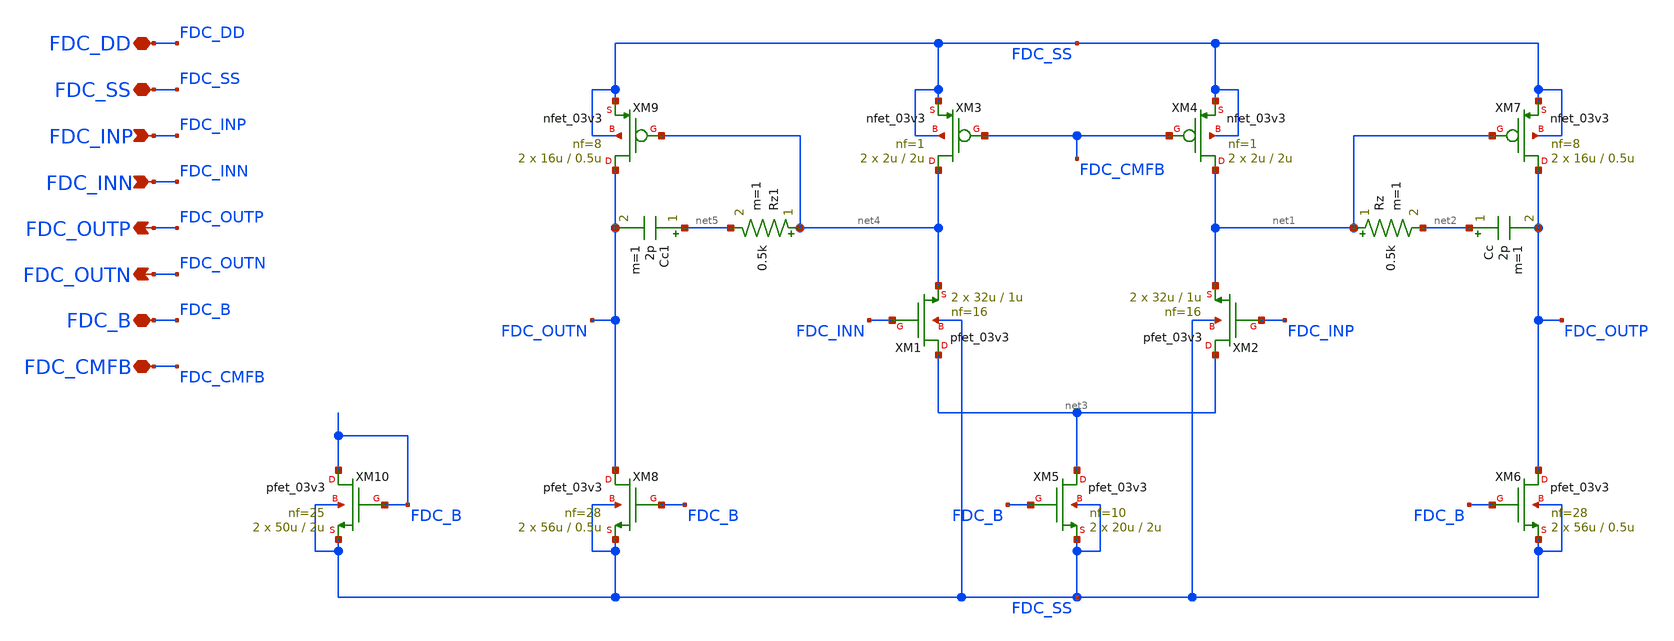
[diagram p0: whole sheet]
** sch_path: Design_Files/IC Design/Schematic/FD_OTA/FDC/FDC.sch
**.subckt FDC FDC_DD FDC_SS FDC_INP FDC_INN FDC_OUTP FDC_B FDC_OUTN FDC_CMFB
*.iopin FDC_DD
*.iopin FDC_SS
*.ipin FDC_INP
*.ipin FDC_INN
*.opin FDC_OUTP
*.iopin FDC_B
*.opin FDC_OUTN
*.iopin FDC_CMFB
XM4 net1 FDC_CMFB FDC_SS FDC_SS nfet_03v3 L=2u W=2u nf=1 ad='int((nf+1)/2) * W/nf * 0.18u' as='int((nf+2)/2) * W/nf * 0.18u'
+ pd='2*int((nf+1)/2) * (W/nf + 0.18u)' ps='2*int((nf+2)/2) * (W/nf + 0.18u)' nrd='0.18u / W' nrs='0.18u / W'
+ sa=0 sb=0 sd=0 m=2
XM3 net4 FDC_CMFB FDC_SS FDC_SS nfet_03v3 L=2u W=2u nf=1 ad='int((nf+1)/2) * W/nf * 0.18u' as='int((nf+2)/2) * W/nf * 0.18u'
+ pd='2*int((nf+1)/2) * (W/nf + 0.18u)' ps='2*int((nf+2)/2) * (W/nf + 0.18u)' nrd='0.18u / W' nrs='0.18u / W'
+ sa=0 sb=0 sd=0 m=2
XM1 net3 FDC_INN net4 FDC_SS pfet_03v3 L=1u W=32u nf=16 ad='int((nf+1)/2) * W/nf * 0.18u' as='int((nf+2)/2) * W/nf * 0.18u'
+ pd='2*int((nf+1)/2) * (W/nf + 0.18u)' ps='2*int((nf+2)/2) * (W/nf + 0.18u)' nrd='0.18u / W' nrs='0.18u / W'
+ sa=0 sb=0 sd=0 m=2
XM2 net3 FDC_INP net1 FDC_SS pfet_03v3 L=1u W=32u nf=16 ad='int((nf+1)/2) * W/nf * 0.18u' as='int((nf+2)/2) * W/nf * 0.18u'
+ pd='2*int((nf+1)/2) * (W/nf + 0.18u)' ps='2*int((nf+2)/2) * (W/nf + 0.18u)' nrd='0.18u / W' nrs='0.18u / W'
+ sa=0 sb=0 sd=0 m=2
XM6 FDC_OUTP FDC_B FDC_SS FDC_SS pfet_03v3 L=0.5u W=56u nf=28 ad='int((nf+1)/2) * W/nf * 0.18u' as='int((nf+2)/2) * W/nf * 0.18u'
+ pd='2*int((nf+1)/2) * (W/nf + 0.18u)' ps='2*int((nf+2)/2) * (W/nf + 0.18u)' nrd='0.18u / W' nrs='0.18u / W'
+ sa=0 sb=0 sd=0 m=2
Rz net1 net2 0.5k m=1
XM5 net3 FDC_B FDC_SS FDC_SS pfet_03v3 L=2u W=20u nf=10 ad='int((nf+1)/2) * W/nf * 0.18u' as='int((nf+2)/2) * W/nf * 0.18u'
+ pd='2*int((nf+1)/2) * (W/nf + 0.18u)' ps='2*int((nf+2)/2) * (W/nf + 0.18u)' nrd='0.18u / W' nrs='0.18u / W'
+ sa=0 sb=0 sd=0 m=2
XM7 FDC_OUTP net1 FDC_SS FDC_SS nfet_03v3 L=0.5u W=16u nf=8 ad='int((nf+1)/2) * W/nf * 0.18u' as='int((nf+2)/2) * W/nf * 0.18u'
+ pd='2*int((nf+1)/2) * (W/nf + 0.18u)' ps='2*int((nf+2)/2) * (W/nf + 0.18u)' nrd='0.18u / W' nrs='0.18u / W'
+ sa=0 sb=0 sd=0 m=2
XM10 FDC_B FDC_B FDC_SS FDC_SS pfet_03v3 L=2u W=50u nf=25 ad='int((nf+1)/2) * W/nf * 0.18u' as='int((nf+2)/2) * W/nf * 0.18u'
+ pd='2*int((nf+1)/2) * (W/nf + 0.18u)' ps='2*int((nf+2)/2) * (W/nf + 0.18u)' nrd='0.18u / W' nrs='0.18u / W'
+ sa=0 sb=0 sd=0 m=2
Cc net2 FDC_OUTP 2p m=1
XM8 FDC_OUTN FDC_B FDC_SS FDC_SS pfet_03v3 L=0.5u W=56u nf=28 ad='int((nf+1)/2) * W/nf * 0.18u' as='int((nf+2)/2) * W/nf * 0.18u'
+ pd='2*int((nf+1)/2) * (W/nf + 0.18u)' ps='2*int((nf+2)/2) * (W/nf + 0.18u)' nrd='0.18u / W' nrs='0.18u / W'
+ sa=0 sb=0 sd=0 m=2
Rz1 net4 net5 0.5k m=1
XM9 FDC_OUTN net4 FDC_SS FDC_SS nfet_03v3 L=0.5u W=16u nf=8 ad='int((nf+1)/2) * W/nf * 0.18u' as='int((nf+2)/2) * W/nf * 0.18u'
+ pd='2*int((nf+1)/2) * (W/nf + 0.18u)' ps='2*int((nf+2)/2) * (W/nf + 0.18u)' nrd='0.18u / W' nrs='0.18u / W'
+ sa=0 sb=0 sd=0 m=2
Cc1 net5 FDC_OUTN 2p m=1
**.ends
.end
